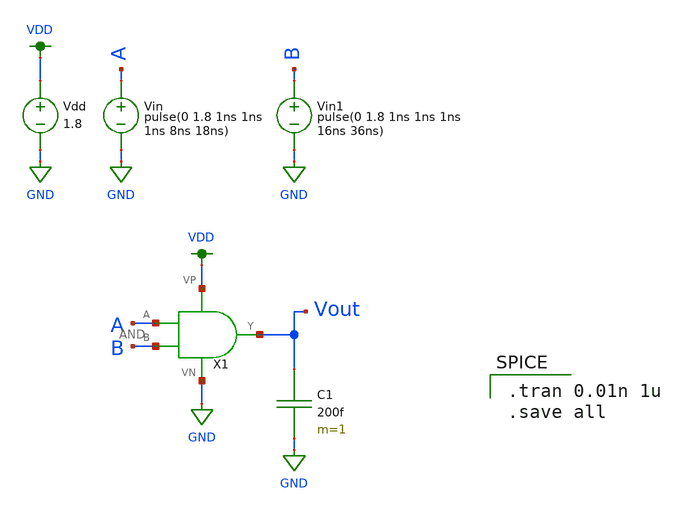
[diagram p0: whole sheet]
** sch_path: MiniProject1-AND/XSCHEM/Test_dock.sch
**.subckt Test_dock
Vdd VDD GND 1.8
Vin A GND pulse(0 1.8 1ns 1ns
1ns 8ns 18ns)
Vin1 B GND pulse(0 1.8 1ns 1ns 1ns
16ns 36ns)
C1 Vout GND 200f m=1
X1 A B VDD GND Vout AND
**** begin user architecture code

.option wnflag=1
.lib ~/skywater/skywater-pdk/libraries/sky130_fd_pr_ngspice/latest/models/sky130.lib.spice tt


.tran 0.01n 1u
.save all

**** end user architecture code
**.ends
.GLOBAL GND
.GLOBAL VDD
.end
